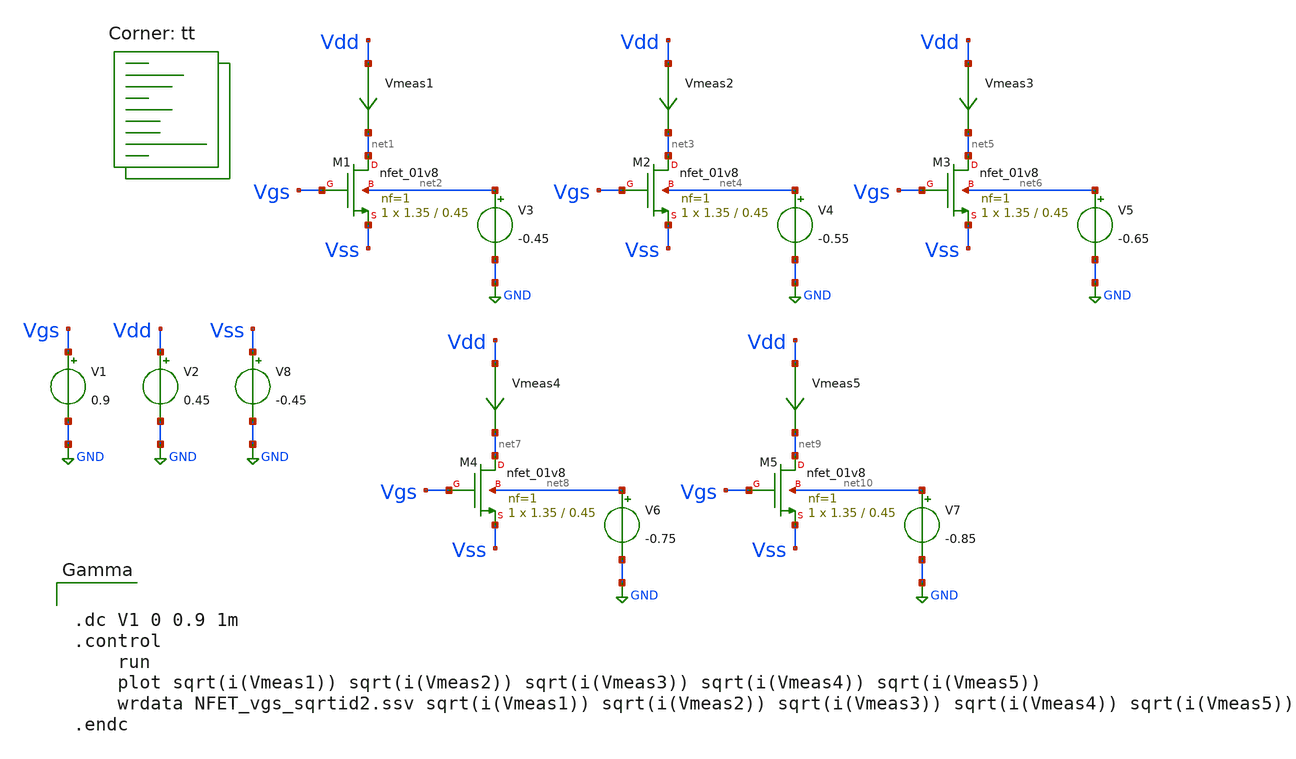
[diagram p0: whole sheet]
** sch_path: opamp_design/Parametros_cmos/NFET_param2.sch
**.subckt NFET_param2
XM1 net1 Vgs Vss net2 sky130_fd_pr__nfet_01v8 L=0.45 W=1.35 nf=1 ad='int((nf+1)/2) * W/nf * 0.29' as='int((nf+2)/2) * W/nf * 0.29'
+ pd='2*int((nf+1)/2) * (W/nf + 0.29)' ps='2*int((nf+2)/2) * (W/nf + 0.29)' nrd='0.29 / W' nrs='0.29 / W'
+ sa=0 sb=0 sd=0 mult=1 m=1
Vmeas1 Vdd net1 0
.save i(vmeas1)
V2 Vdd GND 0.45
V1 Vgs GND 0.9
V3 net2 GND -0.45
XM2 net3 Vgs Vss net4 sky130_fd_pr__nfet_01v8 L=0.45 W=1.35 nf=1 ad='int((nf+1)/2) * W/nf * 0.29' as='int((nf+2)/2) * W/nf * 0.29'
+ pd='2*int((nf+1)/2) * (W/nf + 0.29)' ps='2*int((nf+2)/2) * (W/nf + 0.29)' nrd='0.29 / W' nrs='0.29 / W'
+ sa=0 sb=0 sd=0 mult=1 m=1
Vmeas2 Vdd net3 0
.save i(vmeas2)
V4 net4 GND -0.55
XM3 net5 Vgs Vss net6 sky130_fd_pr__nfet_01v8 L=0.45 W=1.35 nf=1 ad='int((nf+1)/2) * W/nf * 0.29' as='int((nf+2)/2) * W/nf * 0.29'
+ pd='2*int((nf+1)/2) * (W/nf + 0.29)' ps='2*int((nf+2)/2) * (W/nf + 0.29)' nrd='0.29 / W' nrs='0.29 / W'
+ sa=0 sb=0 sd=0 mult=1 m=1
Vmeas3 Vdd net5 0
.save i(vmeas3)
V5 net6 GND -0.65
XM4 net7 Vgs Vss net8 sky130_fd_pr__nfet_01v8 L=0.45 W=1.35 nf=1 ad='int((nf+1)/2) * W/nf * 0.29' as='int((nf+2)/2) * W/nf * 0.29'
+ pd='2*int((nf+1)/2) * (W/nf + 0.29)' ps='2*int((nf+2)/2) * (W/nf + 0.29)' nrd='0.29 / W' nrs='0.29 / W'
+ sa=0 sb=0 sd=0 mult=1 m=1
Vmeas4 Vdd net7 0
.save i(vmeas4)
V6 net8 GND -0.75
XM5 net9 Vgs Vss net10 sky130_fd_pr__nfet_01v8 L=0.45 W=1.35 nf=1 ad='int((nf+1)/2) * W/nf * 0.29' as='int((nf+2)/2) * W/nf * 0.29'
+ pd='2*int((nf+1)/2) * (W/nf + 0.29)' ps='2*int((nf+2)/2) * (W/nf + 0.29)' nrd='0.29 / W' nrs='0.29 / W'
+ sa=0 sb=0 sd=0 mult=1 m=1
Vmeas5 Vdd net9 0
.save i(vmeas5)
V7 net10 GND -0.85
V8 Vss GND -0.45
**** begin user architecture code
.lib $::SKYWATER_MODELS/sky130.lib.spice tt


.dc V1 0 0.9 1m
.control
	run
	plot sqrt(i(Vmeas1)) sqrt(i(Vmeas2)) sqrt(i(Vmeas3)) sqrt(i(Vmeas4)) sqrt(i(Vmeas5))
	wrdata NFET_vgs_sqrtid2.ssv sqrt(i(Vmeas1)) sqrt(i(Vmeas2)) sqrt(i(Vmeas3)) sqrt(i(Vmeas4))
+ sqrt(i(Vmeas5))
.endc


**** end user architecture code
**.ends
.GLOBAL GND
.end
